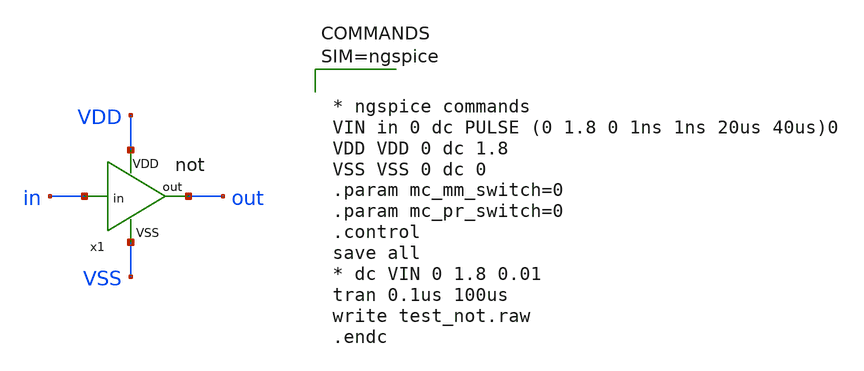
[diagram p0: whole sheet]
** sch_path: xschem/test_not.sch
**.subckt test_not
x1 VDD in out VSS not
**** begin user architecture code



* ngspice commands
VIN in 0 dc PULSE (0 1.8 0 1ns 1ns 20us 40us)0
VDD VDD 0 dc 1.8
VSS VSS 0 dc 0
.param mc_mm_switch=0
.param mc_pr_switch=0
.control
save all
* dc VIN 0 1.8 0.01
tran 0.1us 100us
write test_not.raw
.endc



** opencircuitdesign pdks install
.lib $::SKYWATER_MODELS/sky130.lib.spice tt


**** end user architecture code
**.ends

* expanding   symbol:  not/not.sym # of pins=4
** sym_path: xschem/not/not.sym
** sch_path: xschem/not/not.sch
.subckt not VDD in out VSS
*.ipin in
*.opin out
*.iopin VDD
*.iopin VSS
XM10 out in VDD VDD sky130_fd_pr__pfet_01v8_lvt L=0.35 W=2 nf=1 ad='int((1 + 1)/2) * 2 / 1 * 0.29' as='int((1 + 2)/2) * 2 / 1 * 0.29'
+ pd='2*int((1 + 1)/2) * (2 / 1 + 0.29)' ps='2*int((1 + 2)/2) * (2 / 1 + 0.29)' nrd='0.29 / 2 ' nrs='0.29 / 2 '
+ sa=0 sb=0 sd=0 mult=1 m=1
XM1 out in VSS VSS sky130_fd_pr__nfet_01v8_lvt L=0.35 W=1 nf=1 ad='int((1 + 1)/2) * 1 / 1 * 0.29' as='int((1 + 2)/2) * 1 / 1 * 0.29'
+ pd='2*int((1 + 1)/2) * (1 / 1 + 0.29)' ps='2*int((1 + 2)/2) * (1 / 1 + 0.29)' nrd='0.29 / 1 ' nrs='0.29 / 1 '
+ sa=0 sb=0 sd=0 mult=1 m=1
.ends

.end
